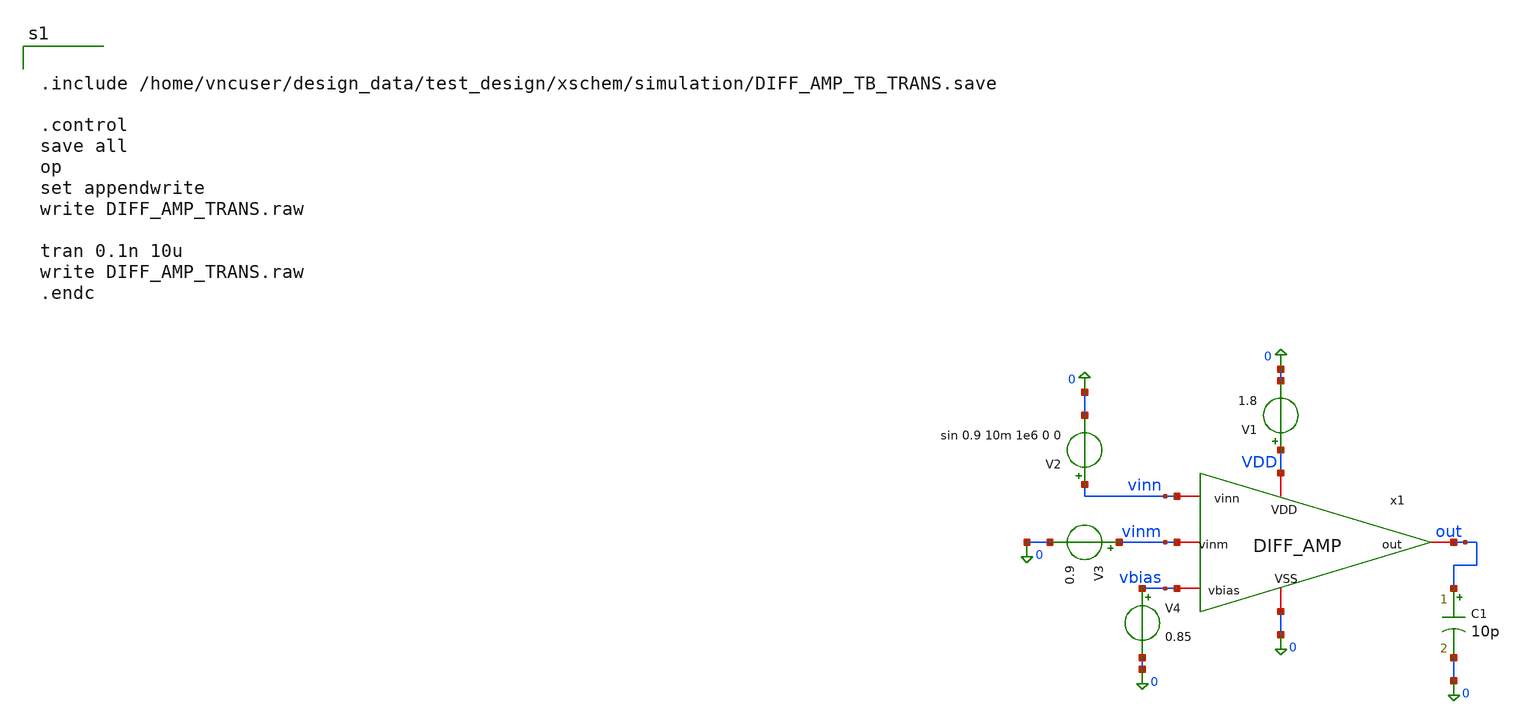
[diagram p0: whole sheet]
** sch_path: OpenAnalogDockSky130/OpenAnalogDockSky130/design_data/test_design/xschem/simulation/DIFF_AMP_TB_TRANS.sch
**.subckt DIFF_AMP_TB_TRANS
x1 VDD vinm vinn vbias 0 out DIFF_AMP
V1 VDD 0 1.8
V2 vinn 0 sin 0.9 10m 1e6 0 0
V3 vinm 0 0.9
V4 vbias 0 0.85
C1 out 0 10p m=1
**** begin user architecture code

** opencircuitdesign pdks install
.lib $::SKYWATER_MODELS/sky130.lib.spice tt



.include /home/vncuser/design_data/test_design/xschem/simulation/DIFF_AMP_TB_TRANS.save

.control
save all
op
set appendwrite
write DIFF_AMP_TRANS.raw

tran 0.1n 10u
write DIFF_AMP_TRANS.raw
.endc


**** end user architecture code
**.ends
.end
